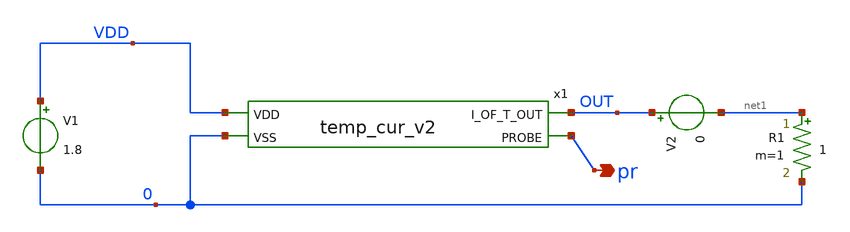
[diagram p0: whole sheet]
** sch_path: design/JNW_GR01_SKY130A/testbench.sch
**.subckt testbench pr
*.opin pr
R1 net1 0 1 m=1
V1 VDD 0 1.8
V2 OUT net1 0
.save i(v2)
x1 VDD OUT pr 0 temp_cur_v2
**.ends
.end
